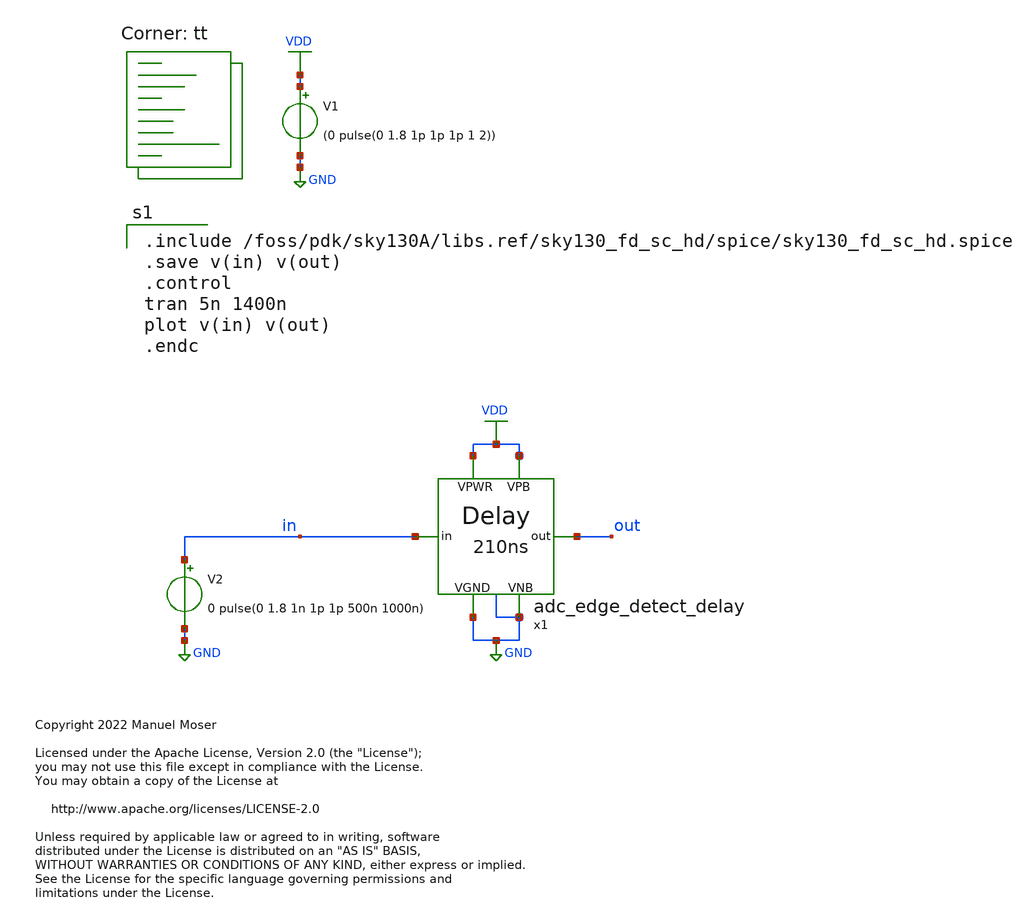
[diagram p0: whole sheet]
** sch_path: archive/xschem/adc_edge_detect_delay/_analog/adc_edge_detect_delay_tb.sch
* Copyright 2022 Manuel Moser
* Licensed under the Apache License, Version 2.0 (the "License");
**.subckt adc_edge_detect_delay_tb
V1 VDD GND (0 pulse(0 1.8 1p 1p 1p 1 2))
V2 in GND 0 pulse(0 1.8 1n 1p 1p 500n 1000n)
x1 GND GND VDD VDD out in adc_edge_detect_delay
**** begin user architecture code

.include /foss/pdk/sky130A/libs.ref/sky130_fd_sc_hd/spice/sky130_fd_sc_hd.spice
.save v(in) v(out)
.control
tran 5n 1400n
plot v(in) v(out)
.endc

.lib $::SKYWATER_MODELS/sky130.lib.spice tt
**** end user architecture code
**.ends

* expanding   symbol:  adc_edge_detect_delay.sym # of pins=6
** sym_path: xschem/adc_edge_detect_delay/adc_edge_detect_delay.sym
** sch_path: xschem/adc_edge_detect_delay/adc_edge_detect_delay.sch
.subckt adc_edge_detect_delay VGND VNB VPB VPWR out in
*.ipin in
*.opin out
*.iopin VPWR
*.iopin VPB
*.iopin VNB
*.iopin VGND
x11 in VGND VNB VPB VPWR net_1 sky130_fd_sc_hd__clkdlybuf4s50_2
x12 net_1 VGND VNB VPB VPWR net_2 sky130_fd_sc_hd__clkdlybuf4s50_2
x13 net_2 VGND VNB VPB VPWR net_3 sky130_fd_sc_hd__clkdlybuf4s50_2
x14 net_3 VGND VNB VPB VPWR net_4 sky130_fd_sc_hd__clkdlybuf4s50_2
x15 net_4 VGND VNB VPB VPWR net_5 sky130_fd_sc_hd__clkdlybuf4s50_2
x16 net_5 VGND VNB VPB VPWR net_6 sky130_fd_sc_hd__clkdlybuf4s50_2
x17 net_6 VGND VNB VPB VPWR net_7 sky130_fd_sc_hd__clkdlybuf4s50_2
x18 net_7 VGND VNB VPB VPWR net_8 sky130_fd_sc_hd__clkdlybuf4s50_2
x19 net_8 VGND VNB VPB VPWR net_9 sky130_fd_sc_hd__clkdlybuf4s50_2
x110 net_9 VGND VNB VPB VPWR net_10 sky130_fd_sc_hd__clkdlybuf4s50_2
x111 net_10 VGND VNB VPB VPWR net_11 sky130_fd_sc_hd__clkdlybuf4s50_2
x112 net_11 VGND VNB VPB VPWR net_12 sky130_fd_sc_hd__clkdlybuf4s50_2
x113 net_12 VGND VNB VPB VPWR net_13 sky130_fd_sc_hd__clkdlybuf4s50_2
x114 net_13 VGND VNB VPB VPWR net_14 sky130_fd_sc_hd__clkdlybuf4s50_2
x115 net_14 VGND VNB VPB VPWR net_15 sky130_fd_sc_hd__clkdlybuf4s50_2
x116 net_15 VGND VNB VPB VPWR net_16 sky130_fd_sc_hd__clkdlybuf4s50_2
x117 net_16 VGND VNB VPB VPWR net_17 sky130_fd_sc_hd__clkdlybuf4s50_2
x118 net_17 VGND VNB VPB VPWR net_18 sky130_fd_sc_hd__clkdlybuf4s50_2
x119 net_18 VGND VNB VPB VPWR net_19 sky130_fd_sc_hd__clkdlybuf4s50_2
x120 net_19 VGND VNB VPB VPWR net_20 sky130_fd_sc_hd__clkdlybuf4s50_2
x121 net_20 VGND VNB VPB VPWR net_21 sky130_fd_sc_hd__clkdlybuf4s50_2
x122 net_21 VGND VNB VPB VPWR net_22 sky130_fd_sc_hd__clkdlybuf4s50_2
x123 net_22 VGND VNB VPB VPWR net_23 sky130_fd_sc_hd__clkdlybuf4s50_2
x124 net_23 VGND VNB VPB VPWR net_24 sky130_fd_sc_hd__clkdlybuf4s50_2
x125 net_24 VGND VNB VPB VPWR net_25 sky130_fd_sc_hd__clkdlybuf4s50_2
x126 net_25 VGND VNB VPB VPWR net_26 sky130_fd_sc_hd__clkdlybuf4s50_2
x127 net_26 VGND VNB VPB VPWR net_27 sky130_fd_sc_hd__clkdlybuf4s50_2
x128 net_27 VGND VNB VPB VPWR net_28 sky130_fd_sc_hd__clkdlybuf4s50_2
x129 net_28 VGND VNB VPB VPWR net_29 sky130_fd_sc_hd__clkdlybuf4s50_2
x130 net_29 VGND VNB VPB VPWR net_30 sky130_fd_sc_hd__clkdlybuf4s50_2
x131 net_30 VGND VNB VPB VPWR net_31 sky130_fd_sc_hd__clkdlybuf4s50_2
x132 net_31 VGND VNB VPB VPWR net_32 sky130_fd_sc_hd__clkdlybuf4s50_2
x133 net_32 VGND VNB VPB VPWR net_33 sky130_fd_sc_hd__clkdlybuf4s50_2
x134 net_33 VGND VNB VPB VPWR net_34 sky130_fd_sc_hd__clkdlybuf4s50_2
x135 net_34 VGND VNB VPB VPWR net_35 sky130_fd_sc_hd__clkdlybuf4s50_2
x136 net_35 VGND VNB VPB VPWR net_36 sky130_fd_sc_hd__clkdlybuf4s50_2
x137 net_36 VGND VNB VPB VPWR net_37 sky130_fd_sc_hd__clkdlybuf4s50_2
x138 net_37 VGND VNB VPB VPWR net_38 sky130_fd_sc_hd__clkdlybuf4s50_2
x139 net_38 VGND VNB VPB VPWR net_39 sky130_fd_sc_hd__clkdlybuf4s50_2
x140 net_39 VGND VNB VPB VPWR net_40 sky130_fd_sc_hd__clkdlybuf4s50_2
x141 net_40 VGND VNB VPB VPWR net_41 sky130_fd_sc_hd__clkdlybuf4s50_2
x142 net_41 VGND VNB VPB VPWR net_42 sky130_fd_sc_hd__clkdlybuf4s50_2
x143 net_42 VGND VNB VPB VPWR net_43 sky130_fd_sc_hd__clkdlybuf4s50_2
x144 net_43 VGND VNB VPB VPWR net_44 sky130_fd_sc_hd__clkdlybuf4s50_2
x145 net_44 VGND VNB VPB VPWR net_45 sky130_fd_sc_hd__clkdlybuf4s50_2
x146 net_45 VGND VNB VPB VPWR net_46 sky130_fd_sc_hd__clkdlybuf4s50_2
x147 net_46 VGND VNB VPB VPWR net_47 sky130_fd_sc_hd__clkdlybuf4s50_2
x148 net_47 VGND VNB VPB VPWR net_48 sky130_fd_sc_hd__clkdlybuf4s50_2
x149 net_48 VGND VNB VPB VPWR net_49 sky130_fd_sc_hd__clkdlybuf4s50_2
x150 net_49 VGND VNB VPB VPWR net_50 sky130_fd_sc_hd__clkdlybuf4s50_2
x151 net_50 VGND VNB VPB VPWR net_51 sky130_fd_sc_hd__clkdlybuf4s50_2
x152 net_51 VGND VNB VPB VPWR net_52 sky130_fd_sc_hd__clkdlybuf4s50_2
x153 net_52 VGND VNB VPB VPWR net_53 sky130_fd_sc_hd__clkdlybuf4s50_2
x154 net_53 VGND VNB VPB VPWR net_54 sky130_fd_sc_hd__clkdlybuf4s50_2
x155 net_54 VGND VNB VPB VPWR net_55 sky130_fd_sc_hd__clkdlybuf4s50_2
x156 net_55 VGND VNB VPB VPWR net_56 sky130_fd_sc_hd__clkdlybuf4s50_2
x157 net_56 VGND VNB VPB VPWR net_57 sky130_fd_sc_hd__clkdlybuf4s50_2
x158 net_57 VGND VNB VPB VPWR net_58 sky130_fd_sc_hd__clkdlybuf4s50_2
x159 net_58 VGND VNB VPB VPWR net_59 sky130_fd_sc_hd__clkdlybuf4s50_2
x160 net_59 VGND VNB VPB VPWR net_60 sky130_fd_sc_hd__clkdlybuf4s50_2
x161 net_60 VGND VNB VPB VPWR net_61 sky130_fd_sc_hd__clkdlybuf4s50_2
x162 net_61 VGND VNB VPB VPWR net_62 sky130_fd_sc_hd__clkdlybuf4s50_2
x163 net_62 VGND VNB VPB VPWR net_63 sky130_fd_sc_hd__clkdlybuf4s50_2
x164 net_63 VGND VNB VPB VPWR net_64 sky130_fd_sc_hd__clkdlybuf4s50_2
x165 net_64 VGND VNB VPB VPWR net_65 sky130_fd_sc_hd__clkdlybuf4s50_2
x166 net_65 VGND VNB VPB VPWR net_66 sky130_fd_sc_hd__clkdlybuf4s50_2
x167 net_66 VGND VNB VPB VPWR net_67 sky130_fd_sc_hd__clkdlybuf4s50_2
x168 net_67 VGND VNB VPB VPWR net_68 sky130_fd_sc_hd__clkdlybuf4s50_2
x169 net_68 VGND VNB VPB VPWR net_69 sky130_fd_sc_hd__clkdlybuf4s50_2
x170 net_69 VGND VNB VPB VPWR net_70 sky130_fd_sc_hd__clkdlybuf4s50_2
x171 net_70 VGND VNB VPB VPWR net_71 sky130_fd_sc_hd__clkdlybuf4s50_2
x172 net_71 VGND VNB VPB VPWR net_72 sky130_fd_sc_hd__clkdlybuf4s50_2
x173 net_72 VGND VNB VPB VPWR net_73 sky130_fd_sc_hd__clkdlybuf4s50_2
x174 net_73 VGND VNB VPB VPWR net_74 sky130_fd_sc_hd__clkdlybuf4s50_2
x175 net_74 VGND VNB VPB VPWR net_75 sky130_fd_sc_hd__clkdlybuf4s50_2
x176 net_75 VGND VNB VPB VPWR net_76 sky130_fd_sc_hd__clkdlybuf4s50_2
x177 net_76 VGND VNB VPB VPWR net_77 sky130_fd_sc_hd__clkdlybuf4s50_2
x178 net_77 VGND VNB VPB VPWR net_78 sky130_fd_sc_hd__clkdlybuf4s50_2
x179 net_78 VGND VNB VPB VPWR net_79 sky130_fd_sc_hd__clkdlybuf4s50_2
x180 net_79 VGND VNB VPB VPWR net_80 sky130_fd_sc_hd__clkdlybuf4s50_2
x181 net_80 VGND VNB VPB VPWR net_81 sky130_fd_sc_hd__clkdlybuf4s50_2
x182 net_81 VGND VNB VPB VPWR net_82 sky130_fd_sc_hd__clkdlybuf4s50_2
x183 net_82 VGND VNB VPB VPWR net_83 sky130_fd_sc_hd__clkdlybuf4s50_2
x184 net_83 VGND VNB VPB VPWR net_84 sky130_fd_sc_hd__clkdlybuf4s50_2
x185 net_84 VGND VNB VPB VPWR net_85 sky130_fd_sc_hd__clkdlybuf4s50_2
x186 net_85 VGND VNB VPB VPWR net_86 sky130_fd_sc_hd__clkdlybuf4s50_2
x187 net_86 VGND VNB VPB VPWR net_87 sky130_fd_sc_hd__clkdlybuf4s50_2
x188 net_87 VGND VNB VPB VPWR net_88 sky130_fd_sc_hd__clkdlybuf4s50_2
x189 net_88 VGND VNB VPB VPWR net_89 sky130_fd_sc_hd__clkdlybuf4s50_2
x190 net_89 VGND VNB VPB VPWR net_90 sky130_fd_sc_hd__clkdlybuf4s50_2
x191 net_90 VGND VNB VPB VPWR net_91 sky130_fd_sc_hd__clkdlybuf4s50_2
x192 net_91 VGND VNB VPB VPWR net_92 sky130_fd_sc_hd__clkdlybuf4s50_2
x193 net_92 VGND VNB VPB VPWR net_93 sky130_fd_sc_hd__clkdlybuf4s50_2
x194 net_93 VGND VNB VPB VPWR net_94 sky130_fd_sc_hd__clkdlybuf4s50_2
x195 net_94 VGND VNB VPB VPWR net_95 sky130_fd_sc_hd__clkdlybuf4s50_2
x196 net_95 VGND VNB VPB VPWR net_96 sky130_fd_sc_hd__clkdlybuf4s50_2
x197 net_96 VGND VNB VPB VPWR net_97 sky130_fd_sc_hd__clkdlybuf4s50_2
x198 net_97 VGND VNB VPB VPWR net_98 sky130_fd_sc_hd__clkdlybuf4s50_2
x199 net_98 VGND VNB VPB VPWR net_99 sky130_fd_sc_hd__clkdlybuf4s50_2
x1100 net_99 VGND VNB VPB VPWR net_100 sky130_fd_sc_hd__clkdlybuf4s50_2
x1101 net_100 VGND VNB VPB VPWR net_101 sky130_fd_sc_hd__clkdlybuf4s50_2
x1102 net_101 VGND VNB VPB VPWR net_102 sky130_fd_sc_hd__clkdlybuf4s50_2
x1103 net_102 VGND VNB VPB VPWR net_103 sky130_fd_sc_hd__clkdlybuf4s50_2
x1104 net_103 VGND VNB VPB VPWR net_104 sky130_fd_sc_hd__clkdlybuf4s50_2
x1105 net_104 VGND VNB VPB VPWR net_105 sky130_fd_sc_hd__clkdlybuf4s50_2
x1106 net_105 VGND VNB VPB VPWR net_106 sky130_fd_sc_hd__clkdlybuf4s50_2
x1107 net_106 VGND VNB VPB VPWR net_107 sky130_fd_sc_hd__clkdlybuf4s50_2
x1108 net_107 VGND VNB VPB VPWR net_108 sky130_fd_sc_hd__clkdlybuf4s50_2
x1109 net_108 VGND VNB VPB VPWR net_109 sky130_fd_sc_hd__clkdlybuf4s50_2
x1110 net_109 VGND VNB VPB VPWR net_110 sky130_fd_sc_hd__clkdlybuf4s50_2
x1111 net_110 VGND VNB VPB VPWR net_111 sky130_fd_sc_hd__clkdlybuf4s50_2
x1112 net_111 VGND VNB VPB VPWR net_112 sky130_fd_sc_hd__clkdlybuf4s50_2
x1113 net_112 VGND VNB VPB VPWR net_113 sky130_fd_sc_hd__clkdlybuf4s50_2
x1114 net_113 VGND VNB VPB VPWR net_114 sky130_fd_sc_hd__clkdlybuf4s50_2
x1115 net_114 VGND VNB VPB VPWR net_115 sky130_fd_sc_hd__clkdlybuf4s50_2
x1116 net_115 VGND VNB VPB VPWR net_116 sky130_fd_sc_hd__clkdlybuf4s50_2
x1117 net_116 VGND VNB VPB VPWR net_117 sky130_fd_sc_hd__clkdlybuf4s50_2
x1118 net_117 VGND VNB VPB VPWR net_118 sky130_fd_sc_hd__clkdlybuf4s50_2
x1119 net_118 VGND VNB VPB VPWR net_119 sky130_fd_sc_hd__clkdlybuf4s50_2
x1120 net_119 VGND VNB VPB VPWR net_120 sky130_fd_sc_hd__clkdlybuf4s50_2
x1121 net_120 VGND VNB VPB VPWR net_121 sky130_fd_sc_hd__clkdlybuf4s50_2
x1122 net_121 VGND VNB VPB VPWR net_122 sky130_fd_sc_hd__clkdlybuf4s50_2
x1123 net_122 VGND VNB VPB VPWR net_123 sky130_fd_sc_hd__clkdlybuf4s50_2
x1124 net_123 VGND VNB VPB VPWR net_124 sky130_fd_sc_hd__clkdlybuf4s50_2
x1125 net_124 VGND VNB VPB VPWR net_125 sky130_fd_sc_hd__clkdlybuf4s50_2
x1126 net_125 VGND VNB VPB VPWR net_126 sky130_fd_sc_hd__clkdlybuf4s50_2
x1127 net_126 VGND VNB VPB VPWR net_127 sky130_fd_sc_hd__clkdlybuf4s50_2
x1128 net_127 VGND VNB VPB VPWR net_128 sky130_fd_sc_hd__clkdlybuf4s50_2
x1129 net_128 VGND VNB VPB VPWR net_129 sky130_fd_sc_hd__clkdlybuf4s50_2
x1130 net_129 VGND VNB VPB VPWR net_130 sky130_fd_sc_hd__clkdlybuf4s50_2
x1131 net_130 VGND VNB VPB VPWR net_131 sky130_fd_sc_hd__clkdlybuf4s50_2
x1132 net_131 VGND VNB VPB VPWR net_132 sky130_fd_sc_hd__clkdlybuf4s50_2
x1133 net_132 VGND VNB VPB VPWR net_133 sky130_fd_sc_hd__clkdlybuf4s50_2
x1134 net_133 VGND VNB VPB VPWR net_134 sky130_fd_sc_hd__clkdlybuf4s50_2
x1135 net_134 VGND VNB VPB VPWR net_135 sky130_fd_sc_hd__clkdlybuf4s50_2
x1136 net_135 VGND VNB VPB VPWR net_136 sky130_fd_sc_hd__clkdlybuf4s50_2
x1137 net_136 VGND VNB VPB VPWR net_137 sky130_fd_sc_hd__clkdlybuf4s50_2
x1138 net_137 VGND VNB VPB VPWR net_138 sky130_fd_sc_hd__clkdlybuf4s50_2
x1139 net_138 VGND VNB VPB VPWR net_139 sky130_fd_sc_hd__clkdlybuf4s50_2
x1140 net_139 VGND VNB VPB VPWR net_140 sky130_fd_sc_hd__clkdlybuf4s50_2
x1141 net_140 VGND VNB VPB VPWR net_141 sky130_fd_sc_hd__clkdlybuf4s50_2
x1142 net_141 VGND VNB VPB VPWR net_142 sky130_fd_sc_hd__clkdlybuf4s50_2
x1143 net_142 VGND VNB VPB VPWR net_143 sky130_fd_sc_hd__clkdlybuf4s50_2
x1144 net_143 VGND VNB VPB VPWR net_144 sky130_fd_sc_hd__clkdlybuf4s50_2
x1145 net_144 VGND VNB VPB VPWR net_145 sky130_fd_sc_hd__clkdlybuf4s50_2
x1146 net_145 VGND VNB VPB VPWR net_146 sky130_fd_sc_hd__clkdlybuf4s50_2
x1147 net_146 VGND VNB VPB VPWR net_147 sky130_fd_sc_hd__clkdlybuf4s50_2
x1148 net_147 VGND VNB VPB VPWR net_148 sky130_fd_sc_hd__clkdlybuf4s50_2
x1149 net_148 VGND VNB VPB VPWR net_149 sky130_fd_sc_hd__clkdlybuf4s50_2
x1150 net_149 VGND VNB VPB VPWR net_150 sky130_fd_sc_hd__clkdlybuf4s50_2
x1151 net_150 VGND VNB VPB VPWR net_151 sky130_fd_sc_hd__clkdlybuf4s50_2
x1152 net_151 VGND VNB VPB VPWR net_152 sky130_fd_sc_hd__clkdlybuf4s50_2
x1153 net_152 VGND VNB VPB VPWR net_153 sky130_fd_sc_hd__clkdlybuf4s50_2
x1154 net_153 VGND VNB VPB VPWR net_154 sky130_fd_sc_hd__clkdlybuf4s50_2
x1155 net_154 VGND VNB VPB VPWR net_155 sky130_fd_sc_hd__clkdlybuf4s50_2
x1156 net_155 VGND VNB VPB VPWR net_156 sky130_fd_sc_hd__clkdlybuf4s50_2
x1157 net_156 VGND VNB VPB VPWR net_157 sky130_fd_sc_hd__clkdlybuf4s50_2
x1158 net_157 VGND VNB VPB VPWR net_158 sky130_fd_sc_hd__clkdlybuf4s50_2
x1159 net_158 VGND VNB VPB VPWR net_159 sky130_fd_sc_hd__clkdlybuf4s50_2
x1160 net_159 VGND VNB VPB VPWR net_160 sky130_fd_sc_hd__clkdlybuf4s50_2
x1161 net_160 VGND VNB VPB VPWR net_161 sky130_fd_sc_hd__clkdlybuf4s50_2
x1162 net_161 VGND VNB VPB VPWR net_162 sky130_fd_sc_hd__clkdlybuf4s50_2
x1163 net_162 VGND VNB VPB VPWR net_163 sky130_fd_sc_hd__clkdlybuf4s50_2
x1164 net_163 VGND VNB VPB VPWR net_164 sky130_fd_sc_hd__clkdlybuf4s50_2
x1165 net_164 VGND VNB VPB VPWR net_165 sky130_fd_sc_hd__clkdlybuf4s50_2
x1166 net_165 VGND VNB VPB VPWR net_166 sky130_fd_sc_hd__clkdlybuf4s50_2
x1167 net_166 VGND VNB VPB VPWR net_167 sky130_fd_sc_hd__clkdlybuf4s50_2
x1168 net_167 VGND VNB VPB VPWR net_168 sky130_fd_sc_hd__clkdlybuf4s50_2
x1169 net_168 VGND VNB VPB VPWR net_169 sky130_fd_sc_hd__clkdlybuf4s50_2
x1170 net_169 VGND VNB VPB VPWR net_170 sky130_fd_sc_hd__clkdlybuf4s50_2
x1171 net_170 VGND VNB VPB VPWR net_171 sky130_fd_sc_hd__clkdlybuf4s50_2
x1172 net_171 VGND VNB VPB VPWR net_172 sky130_fd_sc_hd__clkdlybuf4s50_2
x1173 net_172 VGND VNB VPB VPWR net_173 sky130_fd_sc_hd__clkdlybuf4s50_2
x1174 net_173 VGND VNB VPB VPWR net_174 sky130_fd_sc_hd__clkdlybuf4s50_2
x1175 net_174 VGND VNB VPB VPWR net_175 sky130_fd_sc_hd__clkdlybuf4s50_2
x1176 net_175 VGND VNB VPB VPWR net_176 sky130_fd_sc_hd__clkdlybuf4s50_2
x1177 net_176 VGND VNB VPB VPWR net_177 sky130_fd_sc_hd__clkdlybuf4s50_2
x1178 net_177 VGND VNB VPB VPWR net_178 sky130_fd_sc_hd__clkdlybuf4s50_2
x1179 net_178 VGND VNB VPB VPWR net_179 sky130_fd_sc_hd__clkdlybuf4s50_2
x1180 net_179 VGND VNB VPB VPWR net_180 sky130_fd_sc_hd__clkdlybuf4s50_2
x1181 net_180 VGND VNB VPB VPWR net_181 sky130_fd_sc_hd__clkdlybuf4s50_2
x1182 net_181 VGND VNB VPB VPWR net_182 sky130_fd_sc_hd__clkdlybuf4s50_2
x1183 net_182 VGND VNB VPB VPWR net_183 sky130_fd_sc_hd__clkdlybuf4s50_2
x1184 net_183 VGND VNB VPB VPWR net_184 sky130_fd_sc_hd__clkdlybuf4s50_2
x1185 net_184 VGND VNB VPB VPWR net_185 sky130_fd_sc_hd__clkdlybuf4s50_2
x1186 net_185 VGND VNB VPB VPWR net_186 sky130_fd_sc_hd__clkdlybuf4s50_2
x1187 net_186 VGND VNB VPB VPWR net_187 sky130_fd_sc_hd__clkdlybuf4s50_2
x1188 net_187 VGND VNB VPB VPWR net_188 sky130_fd_sc_hd__clkdlybuf4s50_2
x1189 net_188 VGND VNB VPB VPWR net_189 sky130_fd_sc_hd__clkdlybuf4s50_2
x1190 net_189 VGND VNB VPB VPWR net_190 sky130_fd_sc_hd__clkdlybuf4s50_2
x1191 net_190 VGND VNB VPB VPWR net_191 sky130_fd_sc_hd__clkdlybuf4s50_2
x1192 net_191 VGND VNB VPB VPWR net_192 sky130_fd_sc_hd__clkdlybuf4s50_2
x1193 net_192 VGND VNB VPB VPWR net_193 sky130_fd_sc_hd__clkdlybuf4s50_2
x1194 net_193 VGND VNB VPB VPWR net_194 sky130_fd_sc_hd__clkdlybuf4s50_2
x1195 net_194 VGND VNB VPB VPWR net_195 sky130_fd_sc_hd__clkdlybuf4s50_2
x1196 net_195 VGND VNB VPB VPWR net_196 sky130_fd_sc_hd__clkdlybuf4s50_2
x1197 net_196 VGND VNB VPB VPWR net_197 sky130_fd_sc_hd__clkdlybuf4s50_2
x1198 net_197 VGND VNB VPB VPWR net_198 sky130_fd_sc_hd__clkdlybuf4s50_2
x1199 net_198 VGND VNB VPB VPWR net_199 sky130_fd_sc_hd__clkdlybuf4s50_2
x1200 net_199 VGND VNB VPB VPWR net_200 sky130_fd_sc_hd__clkdlybuf4s50_2
x1201 net_200 VGND VNB VPB VPWR net_201 sky130_fd_sc_hd__clkdlybuf4s50_2
x1202 net_201 VGND VNB VPB VPWR net_202 sky130_fd_sc_hd__clkdlybuf4s50_2
x1203 net_202 VGND VNB VPB VPWR net_203 sky130_fd_sc_hd__clkdlybuf4s50_2
x1204 net_203 VGND VNB VPB VPWR net_204 sky130_fd_sc_hd__clkdlybuf4s50_2
x1205 net_204 VGND VNB VPB VPWR net_205 sky130_fd_sc_hd__clkdlybuf4s50_2
x1206 net_205 VGND VNB VPB VPWR net_206 sky130_fd_sc_hd__clkdlybuf4s50_2
x1207 net_206 VGND VNB VPB VPWR net_207 sky130_fd_sc_hd__clkdlybuf4s50_2
x1208 net_207 VGND VNB VPB VPWR net_208 sky130_fd_sc_hd__clkdlybuf4s50_2
x1209 net_208 VGND VNB VPB VPWR net_209 sky130_fd_sc_hd__clkdlybuf4s50_2
x1210 net_209 VGND VNB VPB VPWR net_210 sky130_fd_sc_hd__clkdlybuf4s50_2
x1211 net_210 VGND VNB VPB VPWR net_211 sky130_fd_sc_hd__clkdlybuf4s50_2
x1212 net_211 VGND VNB VPB VPWR net_212 sky130_fd_sc_hd__clkdlybuf4s50_2
x1213 net_212 VGND VNB VPB VPWR net_213 sky130_fd_sc_hd__clkdlybuf4s50_2
x1214 net_213 VGND VNB VPB VPWR net_214 sky130_fd_sc_hd__clkdlybuf4s50_2
x1215 net_214 VGND VNB VPB VPWR net_215 sky130_fd_sc_hd__clkdlybuf4s50_2
x1216 net_215 VGND VNB VPB VPWR net_216 sky130_fd_sc_hd__clkdlybuf4s50_2
x1217 net_216 VGND VNB VPB VPWR net_217 sky130_fd_sc_hd__clkdlybuf4s50_2
x1218 net_217 VGND VNB VPB VPWR net_218 sky130_fd_sc_hd__clkdlybuf4s50_2
x1219 net_218 VGND VNB VPB VPWR net_219 sky130_fd_sc_hd__clkdlybuf4s50_2
x1220 net_219 VGND VNB VPB VPWR net_220 sky130_fd_sc_hd__clkdlybuf4s50_2
x1221 net_220 VGND VNB VPB VPWR net_221 sky130_fd_sc_hd__clkdlybuf4s50_2
x1222 net_221 VGND VNB VPB VPWR net_222 sky130_fd_sc_hd__clkdlybuf4s50_2
x1223 net_222 VGND VNB VPB VPWR net_223 sky130_fd_sc_hd__clkdlybuf4s50_2
x1224 net_223 VGND VNB VPB VPWR net_224 sky130_fd_sc_hd__clkdlybuf4s50_2
x1225 net_224 VGND VNB VPB VPWR net_225 sky130_fd_sc_hd__clkdlybuf4s50_2
x1226 net_225 VGND VNB VPB VPWR net_226 sky130_fd_sc_hd__clkdlybuf4s50_2
x1227 net_226 VGND VNB VPB VPWR net_227 sky130_fd_sc_hd__clkdlybuf4s50_2
x1228 net_227 VGND VNB VPB VPWR net_228 sky130_fd_sc_hd__clkdlybuf4s50_2
x1229 net_228 VGND VNB VPB VPWR net_229 sky130_fd_sc_hd__clkdlybuf4s50_2
x1230 net_229 VGND VNB VPB VPWR net_230 sky130_fd_sc_hd__clkdlybuf4s50_2
x1231 net_230 VGND VNB VPB VPWR net_231 sky130_fd_sc_hd__clkdlybuf4s50_2
x1232 net_231 VGND VNB VPB VPWR net_232 sky130_fd_sc_hd__clkdlybuf4s50_2
x1233 net_232 VGND VNB VPB VPWR net_233 sky130_fd_sc_hd__clkdlybuf4s50_2
x1234 net_233 VGND VNB VPB VPWR net_234 sky130_fd_sc_hd__clkdlybuf4s50_2
x1235 net_234 VGND VNB VPB VPWR net_235 sky130_fd_sc_hd__clkdlybuf4s50_2
x1236 net_235 VGND VNB VPB VPWR net_236 sky130_fd_sc_hd__clkdlybuf4s50_2
x1237 net_236 VGND VNB VPB VPWR net_237 sky130_fd_sc_hd__clkdlybuf4s50_2
x1238 net_237 VGND VNB VPB VPWR net_238 sky130_fd_sc_hd__clkdlybuf4s50_2
x1239 net_238 VGND VNB VPB VPWR net_239 sky130_fd_sc_hd__clkdlybuf4s50_2
x1240 net_239 VGND VNB VPB VPWR net_240 sky130_fd_sc_hd__clkdlybuf4s50_2
x1241 net_240 VGND VNB VPB VPWR net_241 sky130_fd_sc_hd__clkdlybuf4s50_2
x1242 net_241 VGND VNB VPB VPWR net_242 sky130_fd_sc_hd__clkdlybuf4s50_2
x1243 net_242 VGND VNB VPB VPWR net_243 sky130_fd_sc_hd__clkdlybuf4s50_2
x1244 net_243 VGND VNB VPB VPWR net_244 sky130_fd_sc_hd__clkdlybuf4s50_2
x1245 net_244 VGND VNB VPB VPWR net_245 sky130_fd_sc_hd__clkdlybuf4s50_2
x1246 net_245 VGND VNB VPB VPWR net_246 sky130_fd_sc_hd__clkdlybuf4s50_2
x1247 net_246 VGND VNB VPB VPWR net_247 sky130_fd_sc_hd__clkdlybuf4s50_2
x1248 net_247 VGND VNB VPB VPWR net_248 sky130_fd_sc_hd__clkdlybuf4s50_2
x1249 net_248 VGND VNB VPB VPWR net_249 sky130_fd_sc_hd__clkdlybuf4s50_2
x1250 net_249 VGND VNB VPB VPWR net_250 sky130_fd_sc_hd__clkdlybuf4s50_2
x1251 net_250 VGND VNB VPB VPWR net_251 sky130_fd_sc_hd__clkdlybuf4s50_2
x1252 net_251 VGND VNB VPB VPWR net_252 sky130_fd_sc_hd__clkdlybuf4s50_2
x1253 net_252 VGND VNB VPB VPWR net_253 sky130_fd_sc_hd__clkdlybuf4s50_2
x1254 net_253 VGND VNB VPB VPWR net_254 sky130_fd_sc_hd__clkdlybuf4s50_2
x1255 net_254 VGND VNB VPB VPWR net_255 sky130_fd_sc_hd__clkdlybuf4s50_2
x1256 net_255 VGND VNB VPB VPWR net_256 sky130_fd_sc_hd__clkdlybuf4s50_2
x1257 net_256 VGND VNB VPB VPWR net_257 sky130_fd_sc_hd__clkdlybuf4s50_2
x1258 net_257 VGND VNB VPB VPWR net_258 sky130_fd_sc_hd__clkdlybuf4s50_2
x1259 net_258 VGND VNB VPB VPWR net_259 sky130_fd_sc_hd__clkdlybuf4s50_2
x1260 net_259 VGND VNB VPB VPWR net_260 sky130_fd_sc_hd__clkdlybuf4s50_2
x1261 net_260 VGND VNB VPB VPWR net_261 sky130_fd_sc_hd__clkdlybuf4s50_2
x1262 net_261 VGND VNB VPB VPWR net_262 sky130_fd_sc_hd__clkdlybuf4s50_2
x1263 net_262 VGND VNB VPB VPWR net_263 sky130_fd_sc_hd__clkdlybuf4s50_2
x1264 net_263 VGND VNB VPB VPWR net_264 sky130_fd_sc_hd__clkdlybuf4s50_2
x1265 net_264 VGND VNB VPB VPWR net_265 sky130_fd_sc_hd__clkdlybuf4s50_2
x1266 net_265 VGND VNB VPB VPWR net_266 sky130_fd_sc_hd__clkdlybuf4s50_2
x1267 net_266 VGND VNB VPB VPWR net_267 sky130_fd_sc_hd__clkdlybuf4s50_2
x1268 net_267 VGND VNB VPB VPWR net_268 sky130_fd_sc_hd__clkdlybuf4s50_2
x1269 net_268 VGND VNB VPB VPWR net_269 sky130_fd_sc_hd__clkdlybuf4s50_2
x1270 net_269 VGND VNB VPB VPWR net_270 sky130_fd_sc_hd__clkdlybuf4s50_2
x1271 net_270 VGND VNB VPB VPWR net_271 sky130_fd_sc_hd__clkdlybuf4s50_2
x1272 net_271 VGND VNB VPB VPWR net_272 sky130_fd_sc_hd__clkdlybuf4s50_2
x1273 net_272 VGND VNB VPB VPWR net_273 sky130_fd_sc_hd__clkdlybuf4s50_2
x1274 net_273 VGND VNB VPB VPWR net_274 sky130_fd_sc_hd__clkdlybuf4s50_2
x1275 net_274 VGND VNB VPB VPWR net_275 sky130_fd_sc_hd__clkdlybuf4s50_2
x1276 net_275 VGND VNB VPB VPWR net_276 sky130_fd_sc_hd__clkdlybuf4s50_2
x1277 net_276 VGND VNB VPB VPWR net_277 sky130_fd_sc_hd__clkdlybuf4s50_2
x1278 net_277 VGND VNB VPB VPWR net_278 sky130_fd_sc_hd__clkdlybuf4s50_2
x1279 net_278 VGND VNB VPB VPWR net_279 sky130_fd_sc_hd__clkdlybuf4s50_2
x1280 net_279 VGND VNB VPB VPWR net_280 sky130_fd_sc_hd__clkdlybuf4s50_2
x1281 net_280 VGND VNB VPB VPWR net_281 sky130_fd_sc_hd__clkdlybuf4s50_2
x1282 net_281 VGND VNB VPB VPWR net_282 sky130_fd_sc_hd__clkdlybuf4s50_2
x1283 net_282 VGND VNB VPB VPWR net_283 sky130_fd_sc_hd__clkdlybuf4s50_2
x1284 net_283 VGND VNB VPB VPWR net_284 sky130_fd_sc_hd__clkdlybuf4s50_2
x1285 net_284 VGND VNB VPB VPWR net_285 sky130_fd_sc_hd__clkdlybuf4s50_2
x1286 net_285 VGND VNB VPB VPWR net_286 sky130_fd_sc_hd__clkdlybuf4s50_2
x1287 net_286 VGND VNB VPB VPWR net_287 sky130_fd_sc_hd__clkdlybuf4s50_2
x1288 net_287 VGND VNB VPB VPWR net_288 sky130_fd_sc_hd__clkdlybuf4s50_2
x1289 net_288 VGND VNB VPB VPWR net_289 sky130_fd_sc_hd__clkdlybuf4s50_2
x1290 net_289 VGND VNB VPB VPWR net_290 sky130_fd_sc_hd__clkdlybuf4s50_2
x1291 net_290 VGND VNB VPB VPWR net_291 sky130_fd_sc_hd__clkdlybuf4s50_2
x1292 net_291 VGND VNB VPB VPWR net_292 sky130_fd_sc_hd__clkdlybuf4s50_2
x1293 net_292 VGND VNB VPB VPWR net_293 sky130_fd_sc_hd__clkdlybuf4s50_2
x1294 net_293 VGND VNB VPB VPWR net_294 sky130_fd_sc_hd__clkdlybuf4s50_2
x1295 net_294 VGND VNB VPB VPWR net_295 sky130_fd_sc_hd__clkdlybuf4s50_2
x1296 net_295 VGND VNB VPB VPWR net_296 sky130_fd_sc_hd__clkdlybuf4s50_2
x1297 net_296 VGND VNB VPB VPWR net_297 sky130_fd_sc_hd__clkdlybuf4s50_2
x1298 net_297 VGND VNB VPB VPWR net_298 sky130_fd_sc_hd__clkdlybuf4s50_2
x1299 net_298 VGND VNB VPB VPWR net_299 sky130_fd_sc_hd__clkdlybuf4s50_2
x1300 net_299 VGND VNB VPB VPWR net_300 sky130_fd_sc_hd__clkdlybuf4s50_2
x1301 net_300 VGND VNB VPB VPWR net_301 sky130_fd_sc_hd__clkdlybuf4s50_2
x1302 net_301 VGND VNB VPB VPWR net_302 sky130_fd_sc_hd__clkdlybuf4s50_2
x1303 net_302 VGND VNB VPB VPWR net_303 sky130_fd_sc_hd__clkdlybuf4s50_2
x1304 net_303 VGND VNB VPB VPWR net_304 sky130_fd_sc_hd__clkdlybuf4s50_2
x1305 net_304 VGND VNB VPB VPWR net_305 sky130_fd_sc_hd__clkdlybuf4s50_2
x1306 net_305 VGND VNB VPB VPWR net_306 sky130_fd_sc_hd__clkdlybuf4s50_2
x1307 net_306 VGND VNB VPB VPWR net_307 sky130_fd_sc_hd__clkdlybuf4s50_2
x1308 net_307 VGND VNB VPB VPWR net_308 sky130_fd_sc_hd__clkdlybuf4s50_2
x1309 net_308 VGND VNB VPB VPWR net_309 sky130_fd_sc_hd__clkdlybuf4s50_2
x1310 net_309 VGND VNB VPB VPWR net_310 sky130_fd_sc_hd__clkdlybuf4s50_2
x1311 net_310 VGND VNB VPB VPWR net_311 sky130_fd_sc_hd__clkdlybuf4s50_2
x1312 net_311 VGND VNB VPB VPWR net_312 sky130_fd_sc_hd__clkdlybuf4s50_2
x1313 net_312 VGND VNB VPB VPWR net_313 sky130_fd_sc_hd__clkdlybuf4s50_2
x1314 net_313 VGND VNB VPB VPWR net_314 sky130_fd_sc_hd__clkdlybuf4s50_2
x1315 net_314 VGND VNB VPB VPWR net_315 sky130_fd_sc_hd__clkdlybuf4s50_2
x1316 net_315 VGND VNB VPB VPWR net_316 sky130_fd_sc_hd__clkdlybuf4s50_2
x1317 net_316 VGND VNB VPB VPWR net_317 sky130_fd_sc_hd__clkdlybuf4s50_2
x1318 net_317 VGND VNB VPB VPWR net_318 sky130_fd_sc_hd__clkdlybuf4s50_2
x1319 net_318 VGND VNB VPB VPWR net_319 sky130_fd_sc_hd__clkdlybuf4s50_2
x1320 net_319 VGND VNB VPB VPWR net_320 sky130_fd_sc_hd__clkdlybuf4s50_2
x1321 net_320 VGND VNB VPB VPWR net_321 sky130_fd_sc_hd__clkdlybuf4s50_2
x1322 net_321 VGND VNB VPB VPWR net_322 sky130_fd_sc_hd__clkdlybuf4s50_2
x1323 net_322 VGND VNB VPB VPWR net_323 sky130_fd_sc_hd__clkdlybuf4s50_2
x1324 net_323 VGND VNB VPB VPWR net_324 sky130_fd_sc_hd__clkdlybuf4s50_2
x1325 net_324 VGND VNB VPB VPWR net_325 sky130_fd_sc_hd__clkdlybuf4s50_2
x1326 net_325 VGND VNB VPB VPWR net_326 sky130_fd_sc_hd__clkdlybuf4s50_2
x1327 net_326 VGND VNB VPB VPWR net_327 sky130_fd_sc_hd__clkdlybuf4s50_2
x1328 net_327 VGND VNB VPB VPWR net_328 sky130_fd_sc_hd__clkdlybuf4s50_2
x1329 net_328 VGND VNB VPB VPWR net_329 sky130_fd_sc_hd__clkdlybuf4s50_2
x1330 net_329 VGND VNB VPB VPWR net_330 sky130_fd_sc_hd__clkdlybuf4s50_2
x1331 net_330 VGND VNB VPB VPWR net_331 sky130_fd_sc_hd__clkdlybuf4s50_2
x1332 net_331 VGND VNB VPB VPWR net_332 sky130_fd_sc_hd__clkdlybuf4s50_2
x1333 net_332 VGND VNB VPB VPWR net_333 sky130_fd_sc_hd__clkdlybuf4s50_2
x1334 net_333 VGND VNB VPB VPWR net_334 sky130_fd_sc_hd__clkdlybuf4s50_2
x1335 net_334 VGND VNB VPB VPWR net_335 sky130_fd_sc_hd__clkdlybuf4s50_2
x1336 net_335 VGND VNB VPB VPWR net_336 sky130_fd_sc_hd__clkdlybuf4s50_2
x1337 net_336 VGND VNB VPB VPWR net_337 sky130_fd_sc_hd__clkdlybuf4s50_2
x1338 net_337 VGND VNB VPB VPWR net_338 sky130_fd_sc_hd__clkdlybuf4s50_2
x1339 net_338 VGND VNB VPB VPWR net_339 sky130_fd_sc_hd__clkdlybuf4s50_2
x1340 net_339 VGND VNB VPB VPWR net_340 sky130_fd_sc_hd__clkdlybuf4s50_2
x1341 net_340 VGND VNB VPB VPWR net_341 sky130_fd_sc_hd__clkdlybuf4s50_2
x1342 net_341 VGND VNB VPB VPWR net_342 sky130_fd_sc_hd__clkdlybuf4s50_2
x1343 net_342 VGND VNB VPB VPWR net_343 sky130_fd_sc_hd__clkdlybuf4s50_2
x1344 net_343 VGND VNB VPB VPWR net_344 sky130_fd_sc_hd__clkdlybuf4s50_2
x1345 net_344 VGND VNB VPB VPWR net_345 sky130_fd_sc_hd__clkdlybuf4s50_2
x1346 net_345 VGND VNB VPB VPWR net_346 sky130_fd_sc_hd__clkdlybuf4s50_2
x1347 net_346 VGND VNB VPB VPWR net_347 sky130_fd_sc_hd__clkdlybuf4s50_2
x1348 net_347 VGND VNB VPB VPWR net_348 sky130_fd_sc_hd__clkdlybuf4s50_2
x1349 net_348 VGND VNB VPB VPWR net_349 sky130_fd_sc_hd__clkdlybuf4s50_2
x1350 net_349 VGND VNB VPB VPWR net_350 sky130_fd_sc_hd__clkdlybuf4s50_2
x1351 net_350 VGND VNB VPB VPWR net_351 sky130_fd_sc_hd__clkdlybuf4s50_2
x1352 net_351 VGND VNB VPB VPWR net_352 sky130_fd_sc_hd__clkdlybuf4s50_2
x1353 net_352 VGND VNB VPB VPWR net_353 sky130_fd_sc_hd__clkdlybuf4s50_2
x1354 net_353 VGND VNB VPB VPWR net_354 sky130_fd_sc_hd__clkdlybuf4s50_2
x1355 net_354 VGND VNB VPB VPWR net_355 sky130_fd_sc_hd__clkdlybuf4s50_2
x1356 net_355 VGND VNB VPB VPWR net_356 sky130_fd_sc_hd__clkdlybuf4s50_2
x1357 net_356 VGND VNB VPB VPWR net_357 sky130_fd_sc_hd__clkdlybuf4s50_2
x1358 net_357 VGND VNB VPB VPWR net_358 sky130_fd_sc_hd__clkdlybuf4s50_2
x1359 net_358 VGND VNB VPB VPWR net_359 sky130_fd_sc_hd__clkdlybuf4s50_2
x1360 net_359 VGND VNB VPB VPWR net_360 sky130_fd_sc_hd__clkdlybuf4s50_2
x1361 net_360 VGND VNB VPB VPWR net_361 sky130_fd_sc_hd__clkdlybuf4s50_2
x1362 net_361 VGND VNB VPB VPWR net_362 sky130_fd_sc_hd__clkdlybuf4s50_2
x1363 net_362 VGND VNB VPB VPWR net_363 sky130_fd_sc_hd__clkdlybuf4s50_2
x1364 net_363 VGND VNB VPB VPWR net_364 sky130_fd_sc_hd__clkdlybuf4s50_2
x1365 net_364 VGND VNB VPB VPWR net_365 sky130_fd_sc_hd__clkdlybuf4s50_2
x1366 net_365 VGND VNB VPB VPWR net_366 sky130_fd_sc_hd__clkdlybuf4s50_2
x1367 net_366 VGND VNB VPB VPWR net_367 sky130_fd_sc_hd__clkdlybuf4s50_2
x1368 net_367 VGND VNB VPB VPWR net_368 sky130_fd_sc_hd__clkdlybuf4s50_2
x1369 net_368 VGND VNB VPB VPWR net_369 sky130_fd_sc_hd__clkdlybuf4s50_2
x1370 net_369 VGND VNB VPB VPWR net_370 sky130_fd_sc_hd__clkdlybuf4s50_2
x1371 net_370 VGND VNB VPB VPWR net_371 sky130_fd_sc_hd__clkdlybuf4s50_2
x1372 net_371 VGND VNB VPB VPWR net_372 sky130_fd_sc_hd__clkdlybuf4s50_2
x1373 net_372 VGND VNB VPB VPWR net_373 sky130_fd_sc_hd__clkdlybuf4s50_2
x1374 net_373 VGND VNB VPB VPWR net_374 sky130_fd_sc_hd__clkdlybuf4s50_2
x1375 net_374 VGND VNB VPB VPWR net_375 sky130_fd_sc_hd__clkdlybuf4s50_2
x1376 net_375 VGND VNB VPB VPWR net_376 sky130_fd_sc_hd__clkdlybuf4s50_2
x1377 net_376 VGND VNB VPB VPWR net_377 sky130_fd_sc_hd__clkdlybuf4s50_2
x1378 net_377 VGND VNB VPB VPWR net_378 sky130_fd_sc_hd__clkdlybuf4s50_2
x1379 net_378 VGND VNB VPB VPWR net_379 sky130_fd_sc_hd__clkdlybuf4s50_2
x1380 net_379 VGND VNB VPB VPWR net_380 sky130_fd_sc_hd__clkdlybuf4s50_2
x1381 net_380 VGND VNB VPB VPWR net_381 sky130_fd_sc_hd__clkdlybuf4s50_2
x1382 net_381 VGND VNB VPB VPWR net_382 sky130_fd_sc_hd__clkdlybuf4s50_2
x1383 net_382 VGND VNB VPB VPWR net_383 sky130_fd_sc_hd__clkdlybuf4s50_2
x1384 net_383 VGND VNB VPB VPWR net_384 sky130_fd_sc_hd__clkdlybuf4s50_2
x1385 net_384 VGND VNB VPB VPWR net_385 sky130_fd_sc_hd__clkdlybuf4s50_2
x1386 net_385 VGND VNB VPB VPWR net_386 sky130_fd_sc_hd__clkdlybuf4s50_2
x1387 net_386 VGND VNB VPB VPWR net_387 sky130_fd_sc_hd__clkdlybuf4s50_2
x1388 net_387 VGND VNB VPB VPWR net_388 sky130_fd_sc_hd__clkdlybuf4s50_2
x1389 net_388 VGND VNB VPB VPWR net_389 sky130_fd_sc_hd__clkdlybuf4s50_2
x1390 net_389 VGND VNB VPB VPWR net_390 sky130_fd_sc_hd__clkdlybuf4s50_2
x1391 net_390 VGND VNB VPB VPWR net_391 sky130_fd_sc_hd__clkdlybuf4s50_2
x1392 net_391 VGND VNB VPB VPWR net_392 sky130_fd_sc_hd__clkdlybuf4s50_2
x1393 net_392 VGND VNB VPB VPWR net_393 sky130_fd_sc_hd__clkdlybuf4s50_2
x1394 net_393 VGND VNB VPB VPWR net_394 sky130_fd_sc_hd__clkdlybuf4s50_2
x1395 net_394 VGND VNB VPB VPWR net_395 sky130_fd_sc_hd__clkdlybuf4s50_2
x1396 net_395 VGND VNB VPB VPWR net_396 sky130_fd_sc_hd__clkdlybuf4s50_2
x1397 net_396 VGND VNB VPB VPWR net_397 sky130_fd_sc_hd__clkdlybuf4s50_2
x1398 net_397 VGND VNB VPB VPWR net_398 sky130_fd_sc_hd__clkdlybuf4s50_2
x1399 net_398 VGND VNB VPB VPWR net_399 sky130_fd_sc_hd__clkdlybuf4s50_2
x1400 net_399 VGND VNB VPB VPWR net_400 sky130_fd_sc_hd__clkdlybuf4s50_2
x1401 net_400 VGND VNB VPB VPWR net_401 sky130_fd_sc_hd__clkdlybuf4s50_2
x1402 net_401 VGND VNB VPB VPWR net_402 sky130_fd_sc_hd__clkdlybuf4s50_2
x1403 net_402 VGND VNB VPB VPWR net_403 sky130_fd_sc_hd__clkdlybuf4s50_2
x1404 net_403 VGND VNB VPB VPWR net_404 sky130_fd_sc_hd__clkdlybuf4s50_2
x1405 net_404 VGND VNB VPB VPWR net_405 sky130_fd_sc_hd__clkdlybuf4s50_2
x1406 net_405 VGND VNB VPB VPWR net_406 sky130_fd_sc_hd__clkdlybuf4s50_2
x1407 net_406 VGND VNB VPB VPWR net_407 sky130_fd_sc_hd__clkdlybuf4s50_2
x1408 net_407 VGND VNB VPB VPWR net_408 sky130_fd_sc_hd__clkdlybuf4s50_2
x1409 net_408 VGND VNB VPB VPWR net_409 sky130_fd_sc_hd__clkdlybuf4s50_2
x1410 net_409 VGND VNB VPB VPWR net_410 sky130_fd_sc_hd__clkdlybuf4s50_2
x1411 net_410 VGND VNB VPB VPWR net_411 sky130_fd_sc_hd__clkdlybuf4s50_2
x1412 net_411 VGND VNB VPB VPWR net_412 sky130_fd_sc_hd__clkdlybuf4s50_2
x1413 net_412 VGND VNB VPB VPWR net_413 sky130_fd_sc_hd__clkdlybuf4s50_2
x1414 net_413 VGND VNB VPB VPWR net_414 sky130_fd_sc_hd__clkdlybuf4s50_2
x1415 net_414 VGND VNB VPB VPWR net_415 sky130_fd_sc_hd__clkdlybuf4s50_2
x1416 net_415 VGND VNB VPB VPWR net_416 sky130_fd_sc_hd__clkdlybuf4s50_2
x1417 net_416 VGND VNB VPB VPWR net_417 sky130_fd_sc_hd__clkdlybuf4s50_2
x1418 net_417 VGND VNB VPB VPWR net_418 sky130_fd_sc_hd__clkdlybuf4s50_2
x1419 net_418 VGND VNB VPB VPWR net_419 sky130_fd_sc_hd__clkdlybuf4s50_2
x1420 net_419 VGND VNB VPB VPWR net_420 sky130_fd_sc_hd__clkdlybuf4s50_2
x1421 net_420 VGND VNB VPB VPWR net_421 sky130_fd_sc_hd__clkdlybuf4s50_2
x1422 net_421 VGND VNB VPB VPWR net_422 sky130_fd_sc_hd__clkdlybuf4s50_2
x1423 net_422 VGND VNB VPB VPWR net_423 sky130_fd_sc_hd__clkdlybuf4s50_2
x1424 net_423 VGND VNB VPB VPWR net_424 sky130_fd_sc_hd__clkdlybuf4s50_2
x1425 net_424 VGND VNB VPB VPWR net_425 sky130_fd_sc_hd__clkdlybuf4s50_2
x1426 net_425 VGND VNB VPB VPWR net_426 sky130_fd_sc_hd__clkdlybuf4s50_2
x1427 net_426 VGND VNB VPB VPWR net_427 sky130_fd_sc_hd__clkdlybuf4s50_2
x1428 net_427 VGND VNB VPB VPWR net_428 sky130_fd_sc_hd__clkdlybuf4s50_2
x1429 net_428 VGND VNB VPB VPWR net_429 sky130_fd_sc_hd__clkdlybuf4s50_2
x1430 net_429 VGND VNB VPB VPWR net_430 sky130_fd_sc_hd__clkdlybuf4s50_2
x1431 net_430 VGND VNB VPB VPWR net_431 sky130_fd_sc_hd__clkdlybuf4s50_2
x1432 net_431 VGND VNB VPB VPWR net_432 sky130_fd_sc_hd__clkdlybuf4s50_2
x1433 net_432 VGND VNB VPB VPWR net_433 sky130_fd_sc_hd__clkdlybuf4s50_2
x1434 net_433 VGND VNB VPB VPWR net_434 sky130_fd_sc_hd__clkdlybuf4s50_2
x1435 net_434 VGND VNB VPB VPWR net_435 sky130_fd_sc_hd__clkdlybuf4s50_2
x1436 net_435 VGND VNB VPB VPWR net_436 sky130_fd_sc_hd__clkdlybuf4s50_2
x1437 net_436 VGND VNB VPB VPWR net_437 sky130_fd_sc_hd__clkdlybuf4s50_2
x1438 net_437 VGND VNB VPB VPWR net_438 sky130_fd_sc_hd__clkdlybuf4s50_2
x1439 net_438 VGND VNB VPB VPWR net_439 sky130_fd_sc_hd__clkdlybuf4s50_2
x1440 net_439 VGND VNB VPB VPWR net_440 sky130_fd_sc_hd__clkdlybuf4s50_2
x1441 net_440 VGND VNB VPB VPWR net_441 sky130_fd_sc_hd__clkdlybuf4s50_2
x1442 net_441 VGND VNB VPB VPWR net_442 sky130_fd_sc_hd__clkdlybuf4s50_2
x1443 net_442 VGND VNB VPB VPWR net_443 sky130_fd_sc_hd__clkdlybuf4s50_2
x1444 net_443 VGND VNB VPB VPWR net_444 sky130_fd_sc_hd__clkdlybuf4s50_2
x1445 net_444 VGND VNB VPB VPWR net_445 sky130_fd_sc_hd__clkdlybuf4s50_2
x1446 net_445 VGND VNB VPB VPWR net_446 sky130_fd_sc_hd__clkdlybuf4s50_2
x1447 net_446 VGND VNB VPB VPWR net_447 sky130_fd_sc_hd__clkdlybuf4s50_2
x1448 net_447 VGND VNB VPB VPWR net_448 sky130_fd_sc_hd__clkdlybuf4s50_2
x1449 net_448 VGND VNB VPB VPWR net_449 sky130_fd_sc_hd__clkdlybuf4s50_2
x1450 net_449 VGND VNB VPB VPWR net_450 sky130_fd_sc_hd__clkdlybuf4s50_2
x1451 net_450 VGND VNB VPB VPWR net_451 sky130_fd_sc_hd__clkdlybuf4s50_2
x1452 net_451 VGND VNB VPB VPWR net_452 sky130_fd_sc_hd__clkdlybuf4s50_2
x1453 net_452 VGND VNB VPB VPWR net_453 sky130_fd_sc_hd__clkdlybuf4s50_2
x1454 net_453 VGND VNB VPB VPWR net_454 sky130_fd_sc_hd__clkdlybuf4s50_2
x1455 net_454 VGND VNB VPB VPWR net_455 sky130_fd_sc_hd__clkdlybuf4s50_2
x1456 net_455 VGND VNB VPB VPWR net_456 sky130_fd_sc_hd__clkdlybuf4s50_2
x1457 net_456 VGND VNB VPB VPWR net_457 sky130_fd_sc_hd__clkdlybuf4s50_2
x1458 net_457 VGND VNB VPB VPWR net_458 sky130_fd_sc_hd__clkdlybuf4s50_2
x1459 net_458 VGND VNB VPB VPWR net_459 sky130_fd_sc_hd__clkdlybuf4s50_2
x1460 net_459 VGND VNB VPB VPWR net_460 sky130_fd_sc_hd__clkdlybuf4s50_2
x1461 net_460 VGND VNB VPB VPWR net_461 sky130_fd_sc_hd__clkdlybuf4s50_2
x1462 net_461 VGND VNB VPB VPWR net_462 sky130_fd_sc_hd__clkdlybuf4s50_2
x1463 net_462 VGND VNB VPB VPWR net_463 sky130_fd_sc_hd__clkdlybuf4s50_2
x1464 net_463 VGND VNB VPB VPWR net_464 sky130_fd_sc_hd__clkdlybuf4s50_2
x1465 net_464 VGND VNB VPB VPWR net_465 sky130_fd_sc_hd__clkdlybuf4s50_2
x1466 net_465 VGND VNB VPB VPWR net_466 sky130_fd_sc_hd__clkdlybuf4s50_2
x1467 net_466 VGND VNB VPB VPWR net_467 sky130_fd_sc_hd__clkdlybuf4s50_2
x1468 net_467 VGND VNB VPB VPWR net_468 sky130_fd_sc_hd__clkdlybuf4s50_2
x1469 net_468 VGND VNB VPB VPWR net_469 sky130_fd_sc_hd__clkdlybuf4s50_2
x1470 net_469 VGND VNB VPB VPWR net_470 sky130_fd_sc_hd__clkdlybuf4s50_2
x1471 net_470 VGND VNB VPB VPWR net_471 sky130_fd_sc_hd__clkdlybuf4s50_2
x1472 net_471 VGND VNB VPB VPWR net_472 sky130_fd_sc_hd__clkdlybuf4s50_2
x1473 net_472 VGND VNB VPB VPWR net_473 sky130_fd_sc_hd__clkdlybuf4s50_2
x1474 net_473 VGND VNB VPB VPWR net_474 sky130_fd_sc_hd__clkdlybuf4s50_2
x1475 net_474 VGND VNB VPB VPWR net_475 sky130_fd_sc_hd__clkdlybuf4s50_2
x1476 net_475 VGND VNB VPB VPWR net_476 sky130_fd_sc_hd__clkdlybuf4s50_2
x1477 net_476 VGND VNB VPB VPWR net_477 sky130_fd_sc_hd__clkdlybuf4s50_2
x1478 net_477 VGND VNB VPB VPWR net_478 sky130_fd_sc_hd__clkdlybuf4s50_2
x1479 net_478 VGND VNB VPB VPWR net_479 sky130_fd_sc_hd__clkdlybuf4s50_2
x1480 net_479 VGND VNB VPB VPWR net_480 sky130_fd_sc_hd__clkdlybuf4s50_2
x1481 net_480 VGND VNB VPB VPWR net_481 sky130_fd_sc_hd__clkdlybuf4s50_2
x1482 net_481 VGND VNB VPB VPWR net_482 sky130_fd_sc_hd__clkdlybuf4s50_2
x1483 net_482 VGND VNB VPB VPWR net_483 sky130_fd_sc_hd__clkdlybuf4s50_2
x1484 net_483 VGND VNB VPB VPWR net_484 sky130_fd_sc_hd__clkdlybuf4s50_2
x1485 net_484 VGND VNB VPB VPWR net_485 sky130_fd_sc_hd__clkdlybuf4s50_2
x1486 net_485 VGND VNB VPB VPWR net_486 sky130_fd_sc_hd__clkdlybuf4s50_2
x1487 net_486 VGND VNB VPB VPWR net_487 sky130_fd_sc_hd__clkdlybuf4s50_2
x1488 net_487 VGND VNB VPB VPWR net_488 sky130_fd_sc_hd__clkdlybuf4s50_2
x1489 net_488 VGND VNB VPB VPWR net_489 sky130_fd_sc_hd__clkdlybuf4s50_2
x1490 net_489 VGND VNB VPB VPWR net_490 sky130_fd_sc_hd__clkdlybuf4s50_2
x1491 net_490 VGND VNB VPB VPWR net_491 sky130_fd_sc_hd__clkdlybuf4s50_2
x1492 net_491 VGND VNB VPB VPWR net_492 sky130_fd_sc_hd__clkdlybuf4s50_2
x1493 net_492 VGND VNB VPB VPWR net_493 sky130_fd_sc_hd__clkdlybuf4s50_2
x1494 net_493 VGND VNB VPB VPWR net_494 sky130_fd_sc_hd__clkdlybuf4s50_2
x1495 net_494 VGND VNB VPB VPWR net_495 sky130_fd_sc_hd__clkdlybuf4s50_2
x1496 net_495 VGND VNB VPB VPWR net_496 sky130_fd_sc_hd__clkdlybuf4s50_2
x1497 net_496 VGND VNB VPB VPWR net_497 sky130_fd_sc_hd__clkdlybuf4s50_2
x1498 net_497 VGND VNB VPB VPWR net_498 sky130_fd_sc_hd__clkdlybuf4s50_2
x1499 net_498 VGND VNB VPB VPWR net_499 sky130_fd_sc_hd__clkdlybuf4s50_2
x1500 net_499 VGND VNB VPB VPWR net_500 sky130_fd_sc_hd__clkdlybuf4s50_2
x1501 net_500 VGND VNB VPB VPWR net_501 sky130_fd_sc_hd__clkdlybuf4s50_2
x1502 net_501 VGND VNB VPB VPWR net_502 sky130_fd_sc_hd__clkdlybuf4s50_2
x1503 net_502 VGND VNB VPB VPWR net_503 sky130_fd_sc_hd__clkdlybuf4s50_2
x1504 net_503 VGND VNB VPB VPWR net_504 sky130_fd_sc_hd__clkdlybuf4s50_2
x1505 net_504 VGND VNB VPB VPWR net_505 sky130_fd_sc_hd__clkdlybuf4s50_2
x1506 net_505 VGND VNB VPB VPWR net_506 sky130_fd_sc_hd__clkdlybuf4s50_2
x1507 net_506 VGND VNB VPB VPWR net_507 sky130_fd_sc_hd__clkdlybuf4s50_2
x1508 net_507 VGND VNB VPB VPWR net_508 sky130_fd_sc_hd__clkdlybuf4s50_2
x1509 net_508 VGND VNB VPB VPWR net_509 sky130_fd_sc_hd__clkdlybuf4s50_2
x1510 net_509 VGND VNB VPB VPWR net_510 sky130_fd_sc_hd__clkdlybuf4s50_2
x1511 net_510 VGND VNB VPB VPWR net_511 sky130_fd_sc_hd__clkdlybuf4s50_2
x1512 net_511 VGND VNB VPB VPWR net_512 sky130_fd_sc_hd__clkdlybuf4s50_2
x1513 net_512 VGND VNB VPB VPWR net_513 sky130_fd_sc_hd__clkdlybuf4s50_2
x1514 net_513 VGND VNB VPB VPWR net_514 sky130_fd_sc_hd__clkdlybuf4s50_2
x1515 net_514 VGND VNB VPB VPWR net_515 sky130_fd_sc_hd__clkdlybuf4s50_2
x1516 net_515 VGND VNB VPB VPWR net_516 sky130_fd_sc_hd__clkdlybuf4s50_2
x1517 net_516 VGND VNB VPB VPWR net_517 sky130_fd_sc_hd__clkdlybuf4s50_2
x1518 net_517 VGND VNB VPB VPWR net_518 sky130_fd_sc_hd__clkdlybuf4s50_2
x1519 net_518 VGND VNB VPB VPWR net_519 sky130_fd_sc_hd__clkdlybuf4s50_2
x1520 net_519 VGND VNB VPB VPWR net_520 sky130_fd_sc_hd__clkdlybuf4s50_2
x1521 net_520 VGND VNB VPB VPWR net_521 sky130_fd_sc_hd__clkdlybuf4s50_2
x1522 net_521 VGND VNB VPB VPWR net_522 sky130_fd_sc_hd__clkdlybuf4s50_2
x1523 net_522 VGND VNB VPB VPWR net_523 sky130_fd_sc_hd__clkdlybuf4s50_2
x1524 net_523 VGND VNB VPB VPWR net_524 sky130_fd_sc_hd__clkdlybuf4s50_2
x1525 net_524 VGND VNB VPB VPWR net_525 sky130_fd_sc_hd__clkdlybuf4s50_2
x1526 net_525 VGND VNB VPB VPWR net_526 sky130_fd_sc_hd__clkdlybuf4s50_2
x1527 net_526 VGND VNB VPB VPWR net_527 sky130_fd_sc_hd__clkdlybuf4s50_2
x1528 net_527 VGND VNB VPB VPWR net_528 sky130_fd_sc_hd__clkdlybuf4s50_2
x1529 net_528 VGND VNB VPB VPWR net_529 sky130_fd_sc_hd__clkdlybuf4s50_2
x1530 net_529 VGND VNB VPB VPWR net_530 sky130_fd_sc_hd__clkdlybuf4s50_2
x1531 net_530 VGND VNB VPB VPWR net_531 sky130_fd_sc_hd__clkdlybuf4s50_2
x1532 net_531 VGND VNB VPB VPWR net_532 sky130_fd_sc_hd__clkdlybuf4s50_2
x1533 net_532 VGND VNB VPB VPWR net_533 sky130_fd_sc_hd__clkdlybuf4s50_2
x1534 net_533 VGND VNB VPB VPWR net_534 sky130_fd_sc_hd__clkdlybuf4s50_2
x1535 net_534 VGND VNB VPB VPWR net_535 sky130_fd_sc_hd__clkdlybuf4s50_2
x1536 net_535 VGND VNB VPB VPWR net_536 sky130_fd_sc_hd__clkdlybuf4s50_2
x1537 net_536 VGND VNB VPB VPWR net_537 sky130_fd_sc_hd__clkdlybuf4s50_2
x1538 net_537 VGND VNB VPB VPWR net_538 sky130_fd_sc_hd__clkdlybuf4s50_2
x1539 net_538 VGND VNB VPB VPWR net_539 sky130_fd_sc_hd__clkdlybuf4s50_2
x1540 net_539 VGND VNB VPB VPWR net_540 sky130_fd_sc_hd__clkdlybuf4s50_2
x1541 net_540 VGND VNB VPB VPWR net_541 sky130_fd_sc_hd__clkdlybuf4s50_2
x1542 net_541 VGND VNB VPB VPWR net_542 sky130_fd_sc_hd__clkdlybuf4s50_2
x1543 net_542 VGND VNB VPB VPWR net_543 sky130_fd_sc_hd__clkdlybuf4s50_2
x1544 net_543 VGND VNB VPB VPWR net_544 sky130_fd_sc_hd__clkdlybuf4s50_2
x1545 net_544 VGND VNB VPB VPWR net_545 sky130_fd_sc_hd__clkdlybuf4s50_2
x1546 net_545 VGND VNB VPB VPWR net_546 sky130_fd_sc_hd__clkdlybuf4s50_2
x1547 net_546 VGND VNB VPB VPWR net_547 sky130_fd_sc_hd__clkdlybuf4s50_2
x1548 net_547 VGND VNB VPB VPWR net_548 sky130_fd_sc_hd__clkdlybuf4s50_2
x1549 net_548 VGND VNB VPB VPWR net_549 sky130_fd_sc_hd__clkdlybuf4s50_2
x1550 net_549 VGND VNB VPB VPWR net_550 sky130_fd_sc_hd__clkdlybuf4s50_2
x1551 net_550 VGND VNB VPB VPWR net_551 sky130_fd_sc_hd__clkdlybuf4s50_2
x1552 net_551 VGND VNB VPB VPWR net_552 sky130_fd_sc_hd__clkdlybuf4s50_2
x1553 net_552 VGND VNB VPB VPWR net_553 sky130_fd_sc_hd__clkdlybuf4s50_2
x1554 net_553 VGND VNB VPB VPWR net_554 sky130_fd_sc_hd__clkdlybuf4s50_2
x1555 net_554 VGND VNB VPB VPWR net_555 sky130_fd_sc_hd__clkdlybuf4s50_2
x1556 net_555 VGND VNB VPB VPWR net_556 sky130_fd_sc_hd__clkdlybuf4s50_2
x1557 net_556 VGND VNB VPB VPWR net_557 sky130_fd_sc_hd__clkdlybuf4s50_2
x1558 net_557 VGND VNB VPB VPWR net_558 sky130_fd_sc_hd__clkdlybuf4s50_2
x1559 net_558 VGND VNB VPB VPWR net_559 sky130_fd_sc_hd__clkdlybuf4s50_2
x1560 net_559 VGND VNB VPB VPWR net_560 sky130_fd_sc_hd__clkdlybuf4s50_2
x1561 net_560 VGND VNB VPB VPWR net_561 sky130_fd_sc_hd__clkdlybuf4s50_2
x1562 net_561 VGND VNB VPB VPWR net_562 sky130_fd_sc_hd__clkdlybuf4s50_2
x1563 net_562 VGND VNB VPB VPWR net_563 sky130_fd_sc_hd__clkdlybuf4s50_2
x1564 net_563 VGND VNB VPB VPWR net_564 sky130_fd_sc_hd__clkdlybuf4s50_2
x1565 net_564 VGND VNB VPB VPWR net_565 sky130_fd_sc_hd__clkdlybuf4s50_2
x1566 net_565 VGND VNB VPB VPWR net_566 sky130_fd_sc_hd__clkdlybuf4s50_2
x1567 net_566 VGND VNB VPB VPWR net_567 sky130_fd_sc_hd__clkdlybuf4s50_2
x1568 net_567 VGND VNB VPB VPWR net_568 sky130_fd_sc_hd__clkdlybuf4s50_2
x1569 net_568 VGND VNB VPB VPWR net_569 sky130_fd_sc_hd__clkdlybuf4s50_2
x1570 net_569 VGND VNB VPB VPWR net_570 sky130_fd_sc_hd__clkdlybuf4s50_2
x1571 net_570 VGND VNB VPB VPWR net_571 sky130_fd_sc_hd__clkdlybuf4s50_2
x1572 net_571 VGND VNB VPB VPWR net_572 sky130_fd_sc_hd__clkdlybuf4s50_2
x1573 net_572 VGND VNB VPB VPWR net_573 sky130_fd_sc_hd__clkdlybuf4s50_2
x1574 net_573 VGND VNB VPB VPWR net_574 sky130_fd_sc_hd__clkdlybuf4s50_2
x1575 net_574 VGND VNB VPB VPWR net_575 sky130_fd_sc_hd__clkdlybuf4s50_2
x1576 net_575 VGND VNB VPB VPWR net_576 sky130_fd_sc_hd__clkdlybuf4s50_2
x1577 net_576 VGND VNB VPB VPWR net_577 sky130_fd_sc_hd__clkdlybuf4s50_2
x1578 net_577 VGND VNB VPB VPWR net_578 sky130_fd_sc_hd__clkdlybuf4s50_2
x1579 net_578 VGND VNB VPB VPWR net_579 sky130_fd_sc_hd__clkdlybuf4s50_2
x1580 net_579 VGND VNB VPB VPWR net_580 sky130_fd_sc_hd__clkdlybuf4s50_2
x1581 net_580 VGND VNB VPB VPWR net_581 sky130_fd_sc_hd__clkdlybuf4s50_2
x1582 net_581 VGND VNB VPB VPWR net_582 sky130_fd_sc_hd__clkdlybuf4s50_2
x1583 net_582 VGND VNB VPB VPWR net_583 sky130_fd_sc_hd__clkdlybuf4s50_2
x1584 net_583 VGND VNB VPB VPWR net_584 sky130_fd_sc_hd__clkdlybuf4s50_2
x1585 net_584 VGND VNB VPB VPWR net_585 sky130_fd_sc_hd__clkdlybuf4s50_2
x1586 net_585 VGND VNB VPB VPWR net_586 sky130_fd_sc_hd__clkdlybuf4s50_2
x1587 net_586 VGND VNB VPB VPWR net_587 sky130_fd_sc_hd__clkdlybuf4s50_2
x1588 net_587 VGND VNB VPB VPWR net_588 sky130_fd_sc_hd__clkdlybuf4s50_2
x1589 net_588 VGND VNB VPB VPWR net_589 sky130_fd_sc_hd__clkdlybuf4s50_2
x1590 net_589 VGND VNB VPB VPWR net_590 sky130_fd_sc_hd__clkdlybuf4s50_2
x1591 net_590 VGND VNB VPB VPWR net_591 sky130_fd_sc_hd__clkdlybuf4s50_2
x1592 net_591 VGND VNB VPB VPWR net_592 sky130_fd_sc_hd__clkdlybuf4s50_2
x1593 net_592 VGND VNB VPB VPWR net_593 sky130_fd_sc_hd__clkdlybuf4s50_2
x1594 net_593 VGND VNB VPB VPWR net_594 sky130_fd_sc_hd__clkdlybuf4s50_2
x1595 net_594 VGND VNB VPB VPWR net_595 sky130_fd_sc_hd__clkdlybuf4s50_2
x1596 net_595 VGND VNB VPB VPWR net_596 sky130_fd_sc_hd__clkdlybuf4s50_2
x1597 net_596 VGND VNB VPB VPWR net_597 sky130_fd_sc_hd__clkdlybuf4s50_2
x1598 net_597 VGND VNB VPB VPWR net_598 sky130_fd_sc_hd__clkdlybuf4s50_2
x1599 net_598 VGND VNB VPB VPWR net_599 sky130_fd_sc_hd__clkdlybuf4s50_2
x1600 net_599 VGND VNB VPB VPWR out sky130_fd_sc_hd__clkdlybuf4s50_2
.ends

.GLOBAL VDD
.GLOBAL GND
.end
